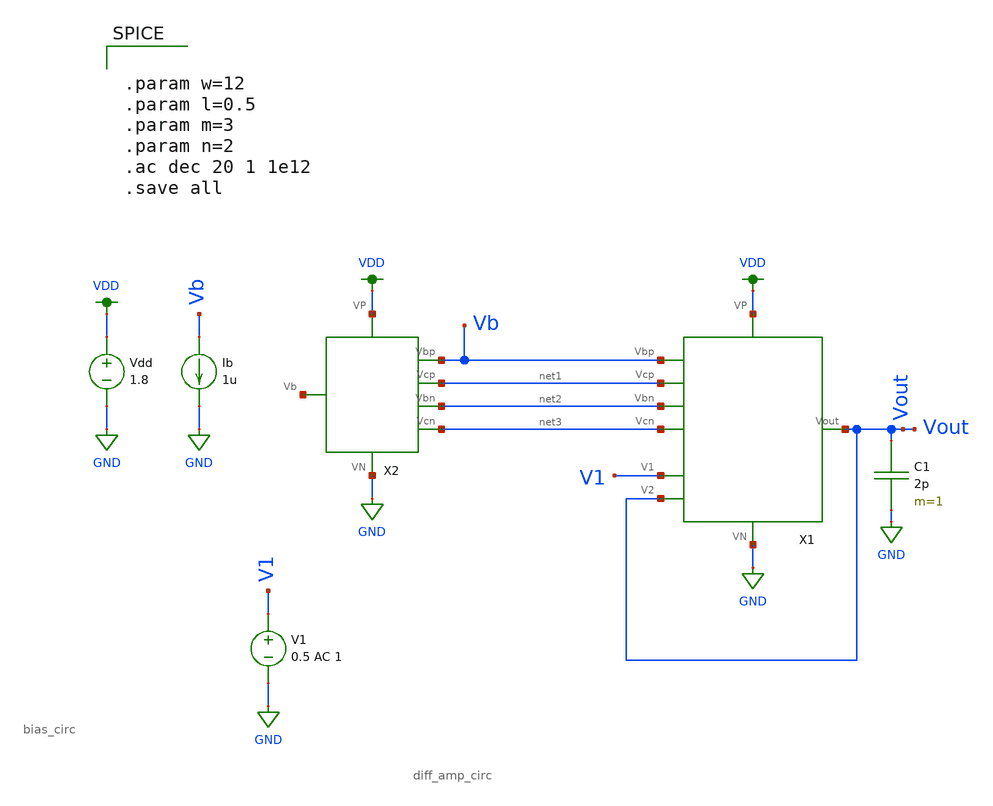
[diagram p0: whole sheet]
** sch_path: Mini_Project_3/diff_amp_unity_gain.sch
**.subckt diff_amp_unity_gain
X2 VDD GND net3 net2 net1 Vb net4 bias_circ
C1 Vout GND 2p m=1
Vdd VDD GND 1.8
Ib Vb GND 1u
X1 Vb net1 net2 net3 Vout GND VDD V1 Vout diff_amp_circ
V1 V1 GND 0.5 AC 1
**** begin user architecture code

.option wnflag=1
.lib ~/skywater/skywater-pdk/libraries/sky130_fd_pr_ngspice/latest/models/sky130.lib.spice tt



.param w=12
.param l=0.5
.param m=3
.param n=2
.ac dec 20 1 1e12
.save all


**** end user architecture code
**.ends
.GLOBAL VDD
.GLOBAL GND
.end
